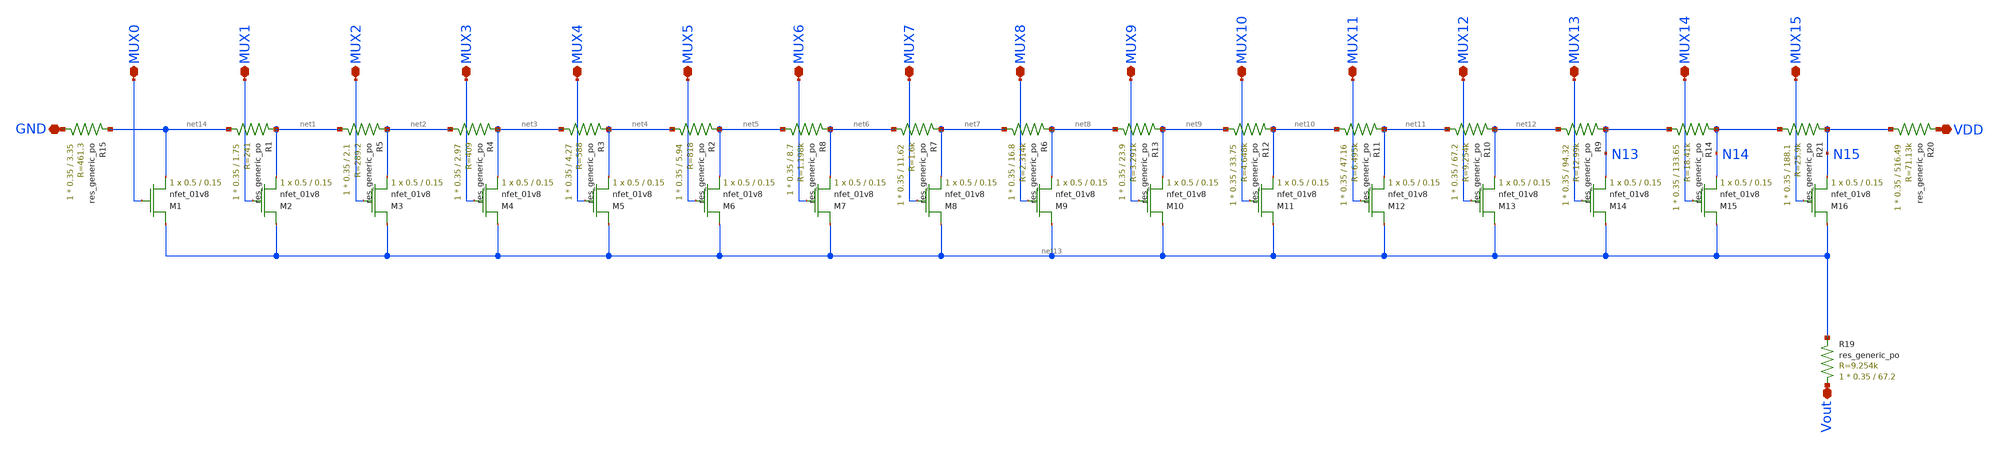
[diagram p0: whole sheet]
** sch_path: DAC/exp_DAC.sch
**.subckt exp_DAC GND MUX0 MUX1 MUX2 MUX3 MUX4 MUX5 MUX6 MUX7 MUX8 MUX9 MUX10 MUX11 MUX12 MUX13
*+ MUX14 MUX15 VDD Vout
*.iopin GND
*.iopin MUX0
*.iopin MUX1
*.iopin MUX2
*.iopin MUX3
*.iopin MUX4
*.iopin MUX5
*.iopin MUX6
*.iopin MUX7
*.iopin MUX8
*.iopin MUX9
*.iopin MUX10
*.iopin MUX11
*.iopin MUX12
*.iopin MUX13
*.iopin MUX14
*.iopin MUX15
*.iopin VDD
*.iopin Vout
XM1 net13 MUX0 net14 GND sky130_fd_pr__nfet_01v8 L=0.15 W=0.5 nf=1 ad='int((nf+1)/2) * W/nf * 0.29' as='int((nf+2)/2) * W/nf * 0.29'
+ pd='2*int((nf+1)/2) * (W/nf + 0.29)' ps='2*int((nf+2)/2) * (W/nf + 0.29)' nrd='0.29 / W' nrs='0.29 / W'
+ sa=0 sb=0 sd=0 mult=1 m=1
XM2 net13 MUX1 net1 GND sky130_fd_pr__nfet_01v8 L=0.15 W=0.5 nf=1 ad='int((nf+1)/2) * W/nf * 0.29' as='int((nf+2)/2) * W/nf * 0.29'
+ pd='2*int((nf+1)/2) * (W/nf + 0.29)' ps='2*int((nf+2)/2) * (W/nf + 0.29)' nrd='0.29 / W' nrs='0.29 / W'
+ sa=0 sb=0 sd=0 mult=1 m=1
XM3 net13 MUX2 net2 GND sky130_fd_pr__nfet_01v8 L=0.15 W=0.5 nf=1 ad='int((nf+1)/2) * W/nf * 0.29' as='int((nf+2)/2) * W/nf * 0.29'
+ pd='2*int((nf+1)/2) * (W/nf + 0.29)' ps='2*int((nf+2)/2) * (W/nf + 0.29)' nrd='0.29 / W' nrs='0.29 / W'
+ sa=0 sb=0 sd=0 mult=1 m=1
XM4 net13 MUX3 net3 GND sky130_fd_pr__nfet_01v8 L=0.15 W=0.5 nf=1 ad='int((nf+1)/2) * W/nf * 0.29' as='int((nf+2)/2) * W/nf * 0.29'
+ pd='2*int((nf+1)/2) * (W/nf + 0.29)' ps='2*int((nf+2)/2) * (W/nf + 0.29)' nrd='0.29 / W' nrs='0.29 / W'
+ sa=0 sb=0 sd=0 mult=1 m=1
XM5 net13 MUX4 net4 GND sky130_fd_pr__nfet_01v8 L=0.15 W=0.5 nf=1 ad='int((nf+1)/2) * W/nf * 0.29' as='int((nf+2)/2) * W/nf * 0.29'
+ pd='2*int((nf+1)/2) * (W/nf + 0.29)' ps='2*int((nf+2)/2) * (W/nf + 0.29)' nrd='0.29 / W' nrs='0.29 / W'
+ sa=0 sb=0 sd=0 mult=1 m=1
XM6 net13 MUX5 net5 GND sky130_fd_pr__nfet_01v8 L=0.15 W=0.5 nf=1 ad='int((nf+1)/2) * W/nf * 0.29' as='int((nf+2)/2) * W/nf * 0.29'
+ pd='2*int((nf+1)/2) * (W/nf + 0.29)' ps='2*int((nf+2)/2) * (W/nf + 0.29)' nrd='0.29 / W' nrs='0.29 / W'
+ sa=0 sb=0 sd=0 mult=1 m=1
XM7 net13 MUX6 net6 GND sky130_fd_pr__nfet_01v8 L=0.15 W=0.5 nf=1 ad='int((nf+1)/2) * W/nf * 0.29' as='int((nf+2)/2) * W/nf * 0.29'
+ pd='2*int((nf+1)/2) * (W/nf + 0.29)' ps='2*int((nf+2)/2) * (W/nf + 0.29)' nrd='0.29 / W' nrs='0.29 / W'
+ sa=0 sb=0 sd=0 mult=1 m=1
XM8 net13 MUX7 net7 GND sky130_fd_pr__nfet_01v8 L=0.15 W=0.5 nf=1 ad='int((nf+1)/2) * W/nf * 0.29' as='int((nf+2)/2) * W/nf * 0.29'
+ pd='2*int((nf+1)/2) * (W/nf + 0.29)' ps='2*int((nf+2)/2) * (W/nf + 0.29)' nrd='0.29 / W' nrs='0.29 / W'
+ sa=0 sb=0 sd=0 mult=1 m=1
XM9 net13 MUX8 net8 GND sky130_fd_pr__nfet_01v8 L=0.15 W=0.5 nf=1 ad='int((nf+1)/2) * W/nf * 0.29' as='int((nf+2)/2) * W/nf * 0.29'
+ pd='2*int((nf+1)/2) * (W/nf + 0.29)' ps='2*int((nf+2)/2) * (W/nf + 0.29)' nrd='0.29 / W' nrs='0.29 / W'
+ sa=0 sb=0 sd=0 mult=1 m=1
XM10 net13 MUX9 net9 GND sky130_fd_pr__nfet_01v8 L=0.15 W=0.5 nf=1 ad='int((nf+1)/2) * W/nf * 0.29' as='int((nf+2)/2) * W/nf * 0.29'
+ pd='2*int((nf+1)/2) * (W/nf + 0.29)' ps='2*int((nf+2)/2) * (W/nf + 0.29)' nrd='0.29 / W' nrs='0.29 / W'
+ sa=0 sb=0 sd=0 mult=1 m=1
XM11 net13 MUX10 net10 GND sky130_fd_pr__nfet_01v8 L=0.15 W=0.5 nf=1 ad='int((nf+1)/2) * W/nf * 0.29'
+ as='int((nf+2)/2) * W/nf * 0.29' pd='2*int((nf+1)/2) * (W/nf + 0.29)' ps='2*int((nf+2)/2) * (W/nf + 0.29)'
+ nrd='0.29 / W' nrs='0.29 / W' sa=0 sb=0 sd=0 mult=1 m=1
XM12 net13 MUX11 net11 GND sky130_fd_pr__nfet_01v8 L=0.15 W=0.5 nf=1 ad='int((nf+1)/2) * W/nf * 0.29'
+ as='int((nf+2)/2) * W/nf * 0.29' pd='2*int((nf+1)/2) * (W/nf + 0.29)' ps='2*int((nf+2)/2) * (W/nf + 0.29)'
+ nrd='0.29 / W' nrs='0.29 / W' sa=0 sb=0 sd=0 mult=1 m=1
XM13 net13 MUX12 net12 GND sky130_fd_pr__nfet_01v8 L=0.15 W=0.5 nf=1 ad='int((nf+1)/2) * W/nf * 0.29'
+ as='int((nf+2)/2) * W/nf * 0.29' pd='2*int((nf+1)/2) * (W/nf + 0.29)' ps='2*int((nf+2)/2) * (W/nf + 0.29)'
+ nrd='0.29 / W' nrs='0.29 / W' sa=0 sb=0 sd=0 mult=1 m=1
XM14 net13 MUX13 N13 GND sky130_fd_pr__nfet_01v8 L=0.15 W=0.5 nf=1 ad='int((nf+1)/2) * W/nf * 0.29' as='int((nf+2)/2) * W/nf * 0.29'
+ pd='2*int((nf+1)/2) * (W/nf + 0.29)' ps='2*int((nf+2)/2) * (W/nf + 0.29)' nrd='0.29 / W' nrs='0.29 / W'
+ sa=0 sb=0 sd=0 mult=1 m=1
XM15 net13 MUX14 N14 GND sky130_fd_pr__nfet_01v8 L=0.15 W=0.5 nf=1 ad='int((nf+1)/2) * W/nf * 0.29' as='int((nf+2)/2) * W/nf * 0.29'
+ pd='2*int((nf+1)/2) * (W/nf + 0.29)' ps='2*int((nf+2)/2) * (W/nf + 0.29)' nrd='0.29 / W' nrs='0.29 / W'
+ sa=0 sb=0 sd=0 mult=1 m=1
XM16 net13 MUX15 N15 GND sky130_fd_pr__nfet_01v8 L=0.15 W=0.5 nf=1 ad='int((nf+1)/2) * W/nf * 0.29' as='int((nf+2)/2) * W/nf * 0.29'
+ pd='2*int((nf+1)/2) * (W/nf + 0.29)' ps='2*int((nf+2)/2) * (W/nf + 0.29)' nrd='0.29 / W' nrs='0.29 / W'
+ sa=0 sb=0 sd=0 mult=1 m=1
XR19 Vout net13 sky130_fd_pr__res_generic_po W=0.35 L=67.2 m=1
XR20 N15 VDD sky130_fd_pr__res_generic_po W=0.35 L=516.49 m=1
XR21 N14 N15 sky130_fd_pr__res_generic_po W=0.35 L=188.1 m=1
XR14 N13 N14 sky130_fd_pr__res_generic_po W=0.35 L=133.65 m=1
XR9 net12 N13 sky130_fd_pr__res_generic_po W=0.35 L=94.32 m=1
XR10 net11 net12 sky130_fd_pr__res_generic_po W=0.35 L=67.2 m=1
XR11 net10 net11 sky130_fd_pr__res_generic_po W=0.35 L=47.16 m=1
XR12 net9 net10 sky130_fd_pr__res_generic_po W=0.35 L=33.75 m=1
XR13 net8 net9 sky130_fd_pr__res_generic_po W=0.35 L=23.9 m=1
XR6 net7 net8 sky130_fd_pr__res_generic_po W=0.35 L=16.8 m=1
XR7 net6 net7 sky130_fd_pr__res_generic_po W=0.35 L=11.62 m=1
XR8 net5 net6 sky130_fd_pr__res_generic_po W=0.35 L=8.7 m=1
XR2 net4 net5 sky130_fd_pr__res_generic_po W=0.35 L=5.94 m=1
XR3 net3 net4 sky130_fd_pr__res_generic_po W=0.35 L=4.27 m=1
XR4 net2 net3 sky130_fd_pr__res_generic_po W=0.35 L=2.97 m=1
XR5 net1 net2 sky130_fd_pr__res_generic_po W=0.35 L=2.1 m=1
XR1 net14 net1 sky130_fd_pr__res_generic_po W=0.35 L=1.75 m=1
XR15 GND net14 sky130_fd_pr__res_generic_po W=0.35 L=3.35 m=1
**.ends
.end
